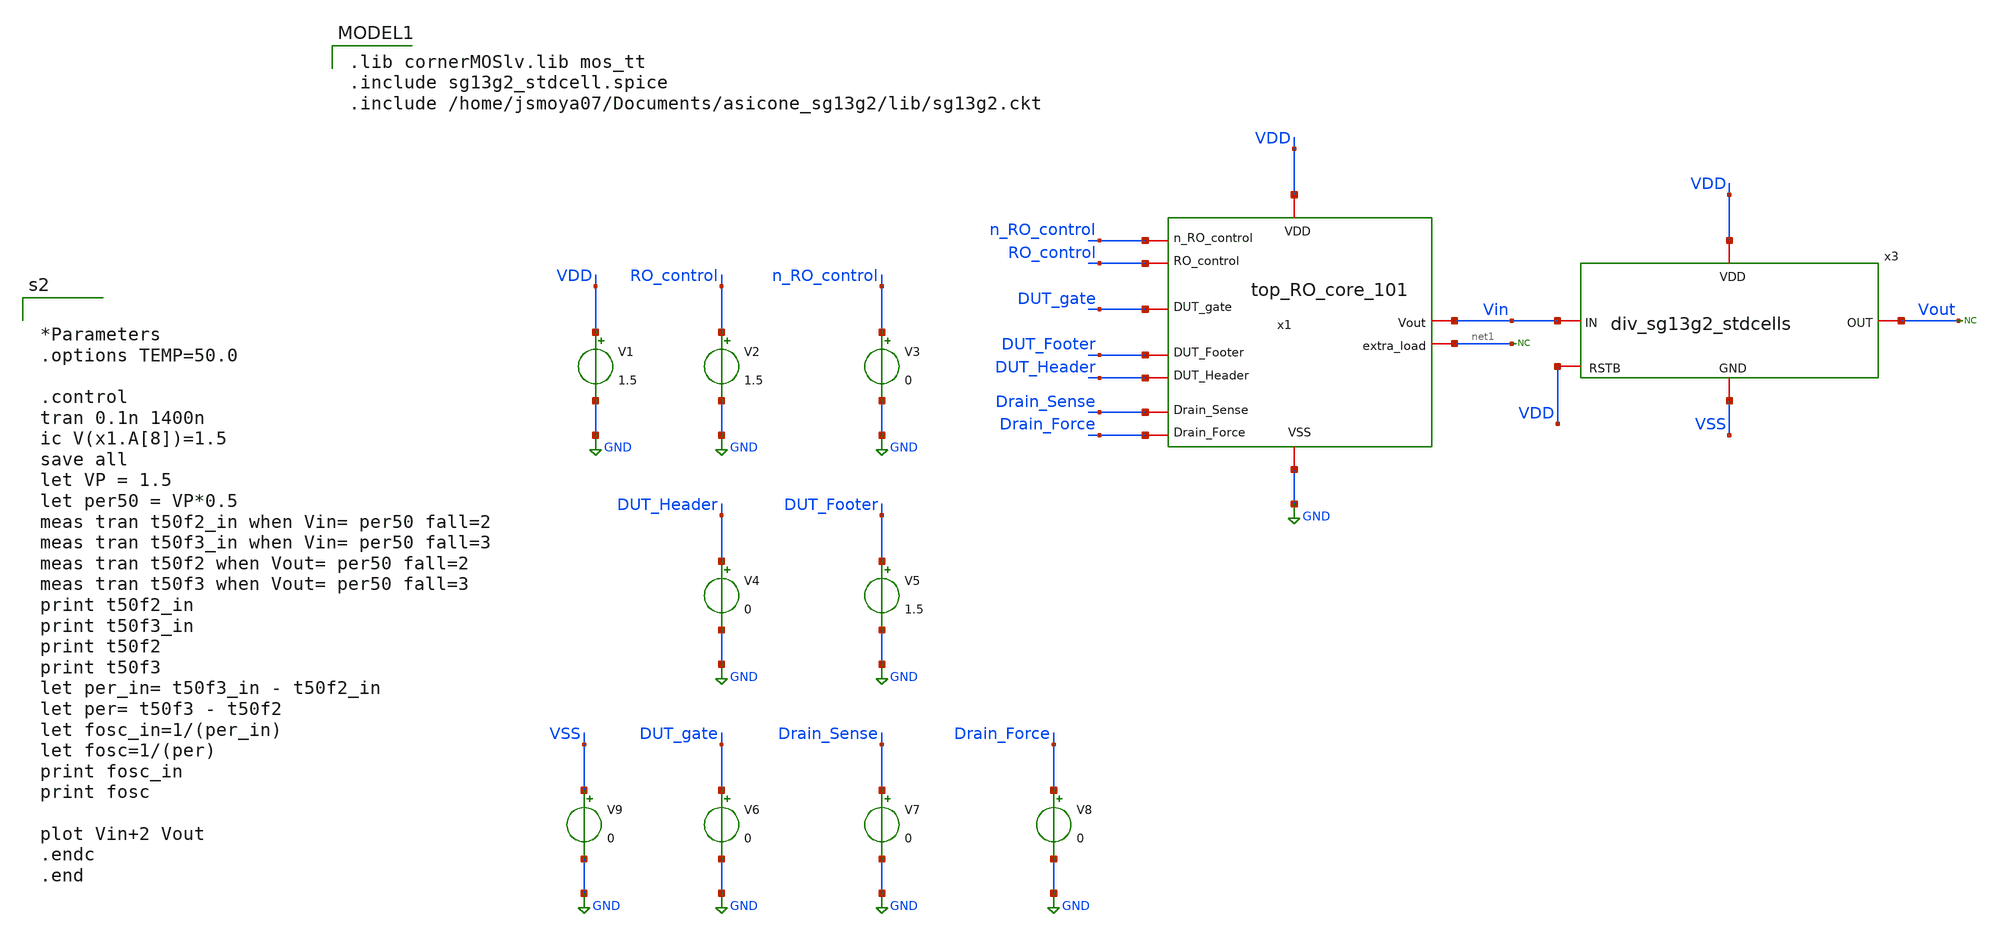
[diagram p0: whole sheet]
** sch_path: unic_cass_wrapper_user_project/ROs_reliability/top_RO_core_101_tb.sch
**.subckt top_RO_core_101_tb
V1 VDD GND 1.5
V2 RO_control GND 1.5
V3 n_RO_control GND 0
V4 DUT_Header GND 0
V5 DUT_Footer GND 1.5
* noconn #net1
V6 DUT_gate GND 0
V7 Drain_Sense GND 0
V8 Drain_Force GND 0
x1 VDD GND n_RO_control RO_control DUT_gate Vin DUT_Header DUT_Footer Drain_Force Drain_Sense net1
+ top_RO_core_101
* noconn Vout
x3 VDD Vout Vin VSS VDD div_sg13g2_stdcells
V9 VSS GND 0
**** begin user architecture code


.ic V(x1.A[8])=0.8
.tran 0.1n 50n
.save all



 .lib cornerMOSlv.lib mos_tt
.include sg13g2_stdcell.spice
.include /home/jsmoya07/Documents/asicone_sg13g2/lib/sg13g2.ckt



*Parameters
.options TEMP=50.0

.control
tran 0.1n 1400n
ic V(x1.A[8])=1.5
save all
let VP = 1.5
let per50 = VP*0.5
meas tran t50f2_in when Vin= per50 fall=2
meas tran t50f3_in when Vin= per50 fall=3
meas tran t50f2 when Vout= per50 fall=2
meas tran t50f3 when Vout= per50 fall=3
print t50f2_in
print t50f3_in
print t50f2
print t50f3
let per_in= t50f3_in - t50f2_in
let per= t50f3 - t50f2
let fosc_in=1/(per_in)
let fosc=1/(per)
print fosc_in
print fosc

plot Vin+2 Vout
.endc
.end


**** end user architecture code
**.ends

* expanding   symbol:  top_RO_core_101.sym # of pins=11
** sym_path: top_RO_core_101.sym
** sch_path: top_RO_core_101.sch
.subckt top_RO_core_101 VDD VSS n_RO_control RO_control DUT_gate Vout DUT_Header DUT_Footer
+ Drain_Force Drain_Sense extra_load
*.iopin VDD
*.iopin VSS
*.iopin n_RO_control
*.iopin RO_control
*.iopin DUT_gate
*.iopin extra_load
*.iopin DUT_Header
*.iopin DUT_Footer
*.iopin Drain_Force
*.iopin Drain_Sense
*.iopin Vout
x1 VDD VSS A[97] A[96] rovcel2
x7 VDD VSS Vout A[100] rovcel2
x3[1] VDD VSS A[96] A[95] rovcel2
x3[2] VDD VSS A[95] A[94] rovcel2
x3[3] VDD VSS A[94] A[93] rovcel2
x3[4] VDD VSS A[93] A[92] rovcel2
x3[5] VDD VSS A[92] A[91] rovcel2
x3[6] VDD VSS A[91] A[90] rovcel2
x3[7] VDD VSS A[90] A[89] rovcel2
x3[8] VDD VSS A[89] A[88] rovcel2
x3[9] VDD VSS A[88] A[87] rovcel2
x3[10] VDD VSS A[87] A[86] rovcel2
x3[11] VDD VSS A[86] A[85] rovcel2
x3[12] VDD VSS A[85] A[84] rovcel2
x3[13] VDD VSS A[84] A[83] rovcel2
x3[14] VDD VSS A[83] A[82] rovcel2
x3[15] VDD VSS A[82] A[81] rovcel2
x3[16] VDD VSS A[81] A[80] rovcel2
x3[17] VDD VSS A[80] A[79] rovcel2
x3[18] VDD VSS A[79] A[78] rovcel2
x3[19] VDD VSS A[78] A[77] rovcel2
x3[20] VDD VSS A[77] A[76] rovcel2
x3[21] VDD VSS A[76] A[75] rovcel2
x3[22] VDD VSS A[75] A[74] rovcel2
x3[23] VDD VSS A[74] A[73] rovcel2
x3[24] VDD VSS A[73] A[72] rovcel2
x3[25] VDD VSS A[72] A[71] rovcel2
x3[26] VDD VSS A[71] A[70] rovcel2
x3[27] VDD VSS A[70] A[69] rovcel2
x3[28] VDD VSS A[69] A[68] rovcel2
x3[29] VDD VSS A[68] A[67] rovcel2
x3[30] VDD VSS A[67] A[66] rovcel2
x3[31] VDD VSS A[66] A[65] rovcel2
x3[32] VDD VSS A[65] A[64] rovcel2
x3[33] VDD VSS A[64] A[63] rovcel2
x3[34] VDD VSS A[63] A[62] rovcel2
x3[35] VDD VSS A[62] A[61] rovcel2
x3[36] VDD VSS A[61] A[60] rovcel2
x3[37] VDD VSS A[60] A[59] rovcel2
x3[38] VDD VSS A[59] A[58] rovcel2
x3[39] VDD VSS A[58] A[57] rovcel2
x3[40] VDD VSS A[57] A[56] rovcel2
x3[41] VDD VSS A[56] A[55] rovcel2
x3[42] VDD VSS A[55] A[54] rovcel2
x3[43] VDD VSS A[54] A[53] rovcel2
x3[44] VDD VSS A[53] A[52] rovcel2
x3[45] VDD VSS A[52] A[51] rovcel2
x3[46] VDD VSS A[51] A[50] rovcel2
x3[47] VDD VSS A[50] A[49] rovcel2
x3[48] VDD VSS A[49] A[48] rovcel2
x3[49] VDD VSS A[48] A[47] rovcel2
x3[50] VDD VSS A[47] A[46] rovcel2
x3[51] VDD VSS A[46] A[45] rovcel2
x3[52] VDD VSS A[45] A[44] rovcel2
x3[53] VDD VSS A[44] A[43] rovcel2
x3[54] VDD VSS A[43] A[42] rovcel2
x3[55] VDD VSS A[42] A[41] rovcel2
x3[56] VDD VSS A[41] A[40] rovcel2
x3[57] VDD VSS A[40] A[39] rovcel2
x3[58] VDD VSS A[39] A[38] rovcel2
x3[59] VDD VSS A[38] A[37] rovcel2
x3[60] VDD VSS A[37] A[36] rovcel2
x3[61] VDD VSS A[36] A[35] rovcel2
x3[62] VDD VSS A[35] A[34] rovcel2
x3[63] VDD VSS A[34] A[33] rovcel2
x3[64] VDD VSS A[33] A[32] rovcel2
x3[65] VDD VSS A[32] A[31] rovcel2
x3[66] VDD VSS A[31] A[30] rovcel2
x3[67] VDD VSS A[30] A[29] rovcel2
x3[68] VDD VSS A[29] A[28] rovcel2
x3[69] VDD VSS A[28] A[27] rovcel2
x3[70] VDD VSS A[27] A[26] rovcel2
x3[71] VDD VSS A[26] A[25] rovcel2
x3[72] VDD VSS A[25] A[24] rovcel2
x3[73] VDD VSS A[24] A[23] rovcel2
x3[74] VDD VSS A[23] A[22] rovcel2
x3[75] VDD VSS A[22] A[21] rovcel2
x3[76] VDD VSS A[21] A[20] rovcel2
x3[77] VDD VSS A[20] A[19] rovcel2
x3[78] VDD VSS A[19] A[18] rovcel2
x3[79] VDD VSS A[18] A[17] rovcel2
x3[80] VDD VSS A[17] A[16] rovcel2
x3[81] VDD VSS A[16] A[15] rovcel2
x3[82] VDD VSS A[15] A[14] rovcel2
x3[83] VDD VSS A[14] A[13] rovcel2
x3[84] VDD VSS A[13] A[12] rovcel2
x3[85] VDD VSS A[12] A[11] rovcel2
x3[86] VDD VSS A[11] A[10] rovcel2
x3[87] VDD VSS A[10] A[9] rovcel2
x3[88] VDD VSS A[9] A[8] rovcel2
x3[89] VDD VSS A[8] A[7] rovcel2
x3[90] VDD VSS A[7] A[6] rovcel2
x3[91] VDD VSS A[6] A[5] rovcel2
x3[92] VDD VSS A[5] A[4] rovcel2
x3[93] VDD VSS A[4] A[3] rovcel2
x3[94] VDD VSS A[3] A[2] rovcel2
x3[95] VDD VSS A[2] A[1] rovcel2
x3[96] VDD VSS A[1] Vout rovcel2
x3 VDD VSS A[97] n_RO_control A[98] RO_control DUT_gate rovcel3
x2 DUT_Header DUT_Footer Drain_Force Drain_Sense RO_control n_RO_control VDD VSS A[98] extra_load
+ rovcel1
x4 VDD VSS extra_load n_RO_control A[100] rovcel4
.ends


* expanding   symbol:  /home/jsmoya07/Documents/RO_reliability/xschem/div_sg13g2_stdcells.sym # of
*+ pins=5
** sym_path: unic_cass_wrapper_user_project/ROs_reliability/div_sg13g2_stdcells.sym
** sch_path: unic_cass_wrapper_user_project/ROs_reliability/div_sg13g2_stdcells.sch
.subckt div_sg13g2_stdcells VDD OUT IN GND RSTB
*.iopin GND
*.iopin IN
*.iopin VDD
*.iopin OUT
*.iopin RSTB
x2 q2 qn2 q1 qn2 RSTB VDD GND sg13g2_dfrbp_1
x1 q1 qn1 IN qn1 RSTB VDD GND sg13g2_dfrbp_1
x3 q3 qn3 q2 qn3 RSTB VDD GND sg13g2_dfrbp_1
x4 q4 qn4 q3 qn4 RSTB VDD GND sg13g2_dfrbp_1
x5 OUT qn5 q4 qn5 RSTB VDD GND sg13g2_dfrbp_1
.ends


* expanding   symbol:  rovcel2.sym # of pins=4
** sym_path: rovcel2.sym
** sch_path: rovcel2.sch
.subckt rovcel2 VDD VSS Vout Vin
*.iopin VDD
*.iopin VSS
*.iopin Vin
*.iopin Vout
* noconn #net1
* noconn #net2
x5 VDD Vin Vout VSS inverter_RO_rel
x1 VDD VDD Vout net2 VSS VSS tgate
x3 VDD VDD Vout net1 VSS VSS tgate
.ends


* expanding   symbol:  rovcel3.sym # of pins=7
** sym_path: rovcel3.sym
** sch_path: rovcel3.sch
.subckt rovcel3 VDD VSS Vin n_RO_control Vout RO_control DUT_gate
*.iopin VDD
*.iopin VSS
*.iopin Vin
*.iopin n_RO_control
*.iopin RO_control
*.iopin DUT_gate
*.iopin Vout
* noconn #net1
x4 VDD VSS Vin n_RO_control RO_control Vout tristate_inv
x1 RO_control VDD Vout net1 VSS n_RO_control tgate
x5 RO_control VDD Vout DUT_gate VSS n_RO_control tgate
.ends


* expanding   symbol:  rovcel1.sym # of pins=10
** sym_path: rovcel1.sym
** sch_path: rovcel1.sch
.subckt rovcel1 DUT_Header DUT_Footer Drain_Force Drain_Sense RO_control n_RO_control VDD VSS Vin
+ Vout
*.iopin VDD
*.iopin VSS
*.iopin Vin
*.iopin DUT_Header
*.iopin DUT_Footer
*.iopin Drain_Force
*.iopin Vout
*.iopin Drain_Sense
*.iopin RO_control
*.iopin n_RO_control
x4 VDD VSS Vin DUT_Header DUT_Footer Vout tristate_inv
x1 RO_control VDD Vout Drain_Force VSS n_RO_control tgate_force
x3 RO_control VDD Vout Drain_Sense VSS n_RO_control tgate
.ends


* expanding   symbol:  rovcel4.sym # of pins=5
** sym_path: rovcel4.sym
** sch_path: rovcel4.sch
.subckt rovcel4 VDD VSS Vin n_RO_control Vout
*.iopin VDD
*.iopin VSS
*.iopin Vin
*.iopin n_RO_control
*.iopin Vout
* noconn #net1
x4 n_RO_control VDD VSS Vin Vout inv1
x1 VDD VDD Vout VSS VSS VSS tgate
x5 VDD VDD Vout net1 VSS VSS tgate
.ends


* expanding   symbol:  sg13g2_stdcells/sg13g2_dfrbp_1.sym # of pins=5
** sym_path: sg13g2_stdcells/sg13g2_dfrbp_1.sym
** sch_path: sg13g2_stdcells/sg13g2_dfrbp_1.sch
.subckt sg13g2_dfrbp_1 Q Q_N CLK D RESET_B VDD VSS
*.ipin D
*.ipin RESET_B
*.ipin CLK
*.opin Q
*.opin Q_N
*.iopin VDD
*.iopin VSS
XM1 Db D net10 VSS sg13_lv_nmos w=420.00n l=130.00n ng=1 m=1 mm_ok=1
XM2 net10 RESET_B VSS VSS sg13_lv_nmos w=420.00n l=130.00n ng=1 m=1 mm_ok=1
XM3 net1 clkneg net9 VSS sg13_lv_nmos w=420.00n l=130.00n ng=1 m=1 mm_ok=1
XM4 net9 net1 VSS VSS sg13_lv_nmos w=420.00n l=130.00n ng=1 m=1 mm_ok=1
XM5 net1 net1 net5 VSS sg13_lv_nmos w=420.00n l=130.00n ng=1 m=1 mm_ok=1
XM6 net5 RESET_B VSS VSS sg13_lv_nmos w=420.00n l=130.00n ng=1 m=1 mm_ok=1
XM7 Q_N net1 VSS VSS sg13_lv_nmos w=740.00n l=130.00n ng=1 m=1 mm_ok=1
XM8 net2 net1 VSS VSS sg13_lv_nmos w=740.00n l=130.00n ng=1 m=1 mm_ok=1
XM9 Q net2 VSS VSS sg13_lv_nmos w=740.00n l=130.00n ng=1 m=1 mm_ok=1
XM10 clkneg CLK VSS VSS sg13_lv_nmos w=740.00n l=130.00n ng=1 m=1 mm_ok=1
XM11 clkpos clkneg VSS VSS sg13_lv_nmos w=740.00n l=130.00n ng=1 m=1 mm_ok=1
XM12 Db clkneg net3 VSS sg13_lv_nmos w=420.00n l=130.00n ng=1 m=1 mm_ok=1
XM13 net3 clkpos net8 VSS sg13_lv_nmos w=420.00n l=130.00n ng=1 m=1 mm_ok=1
XM14 net8 net3 net4 VSS sg13_lv_nmos w=420.00n l=130.00n ng=1 m=1 mm_ok=1
XM15 net4 RESET_B VSS VSS sg13_lv_nmos w=420.00n l=130.00n ng=1 m=1 mm_ok=1
XM16 net3 net3 VSS VSS sg13_lv_nmos w=740.00n l=130.00n ng=1 m=1 mm_ok=1
XM17 net3 clkpos net1 VSS sg13_lv_nmos w=740.00n l=130.00n ng=1 m=1 mm_ok=1
XM18 Db RESET_B VDD VDD sg13_lv_pmos w=420.00n l=130.00n ng=1 m=1 mm_ok=1
XM19 Db D VDD VDD sg13_lv_pmos w=420.00n l=130.00n ng=1 m=1 mm_ok=1
XM20 net7 net1 VDD VDD sg13_lv_pmos w=420.00n l=130.00n ng=1 m=1 mm_ok=1
XM21 net1 clkpos net7 VDD sg13_lv_pmos w=420.00n l=130.00n ng=1 m=1 mm_ok=1
XM22 net1 net1 VDD VDD sg13_lv_pmos w=420.00n l=130.00n ng=1 m=1 mm_ok=1
XM23 net1 RESET_B VDD VDD sg13_lv_pmos w=420.00n l=130.00n ng=1 m=1 mm_ok=1
XM24 Q_N net1 VDD VDD sg13_lv_pmos w=1.12u l=130.00n ng=1 m=1 mm_ok=1
XM25 net2 net1 VDD VDD sg13_lv_pmos w=1.12u l=130.00n ng=1 m=1 mm_ok=1
XM26 Q net2 VDD VDD sg13_lv_pmos w=1.12u l=130.00n ng=1 m=1 mm_ok=1
XM27 clkneg CLK VDD VDD sg13_lv_pmos w=1.12u l=130.00n ng=1 m=1 mm_ok=1
XM28 clkpos clkneg VDD VDD sg13_lv_pmos w=1.12u l=130.00n ng=1 m=1 mm_ok=1
XM29 Db clkpos net3 VDD sg13_lv_pmos w=420.00n l=130.00n ng=1 m=1 mm_ok=1
XM30 net6 net3 VDD VDD sg13_lv_pmos w=420.00n l=130.00n ng=1 m=1 mm_ok=1
XM31 net3 clkneg net6 VDD sg13_lv_pmos w=420.00n l=130.00n ng=1 m=1 mm_ok=1
XM32 net3 RESET_B VDD VDD sg13_lv_pmos w=420.00n l=130.00n ng=1 m=1 mm_ok=1
XM33 net3 net3 VDD VDD sg13_lv_pmos w=1.000u l=130.00n ng=1 m=1 mm_ok=1
XM34 net3 clkneg net1 VDD sg13_lv_pmos w=1.000u l=130.00n ng=1 m=1 mm_ok=1
.ends


* expanding   symbol:  inverter_RO_rel.sym # of pins=4
** sym_path: inverter_RO_rel.sym
** sch_path: inverter_RO_rel.sch
.subckt inverter_RO_rel VDD Vin Vout VSS
*.iopin VDD
*.iopin VSS
*.iopin Vin
*.iopin Vout
XM3 Vout Vin VDD VDD sg13_lv_pmos w=3.4u l=0.45u ng=1 m=4 mm_ok=1
XM1 VSS Vin Vout VSS sg13_lv_nmos w=1.3u l=0.45u ng=1 m=4 mm_ok=1
.ends


* expanding   symbol:  tgate.sym # of pins=6
** sym_path: tgate.sym
** sch_path: tgate.sch
.subckt tgate nclk VDD Vin Vout VSS clk
*.iopin nclk
*.iopin clk
*.iopin VDD
*.iopin VSS
*.iopin Vout
*.iopin Vin
XM3 Vout nclk Vin VDD sg13_lv_pmos w=3.4u l=0.45u ng=1 m=1 mm_ok=1
XM1 Vout clk Vin VSS sg13_lv_nmos w=1.3u l=0.45u ng=1 m=1 mm_ok=1
.ends


* expanding   symbol:  tristate_inv.sym # of pins=6
** sym_path: tristate_inv.sym
** sch_path: tristate_inv.sch
.subckt tristate_inv VDD VSS Vin Vup Vdn Vout
*.iopin VDD
*.iopin VSS
*.iopin Vin
*.iopin Vout
*.iopin Vup
*.iopin Vdn
XM5 Vout Vin net1 VDD sg13_lv_pmos w=3.4u l=0.45u ng=1 m=4 mm_ok=1
XM2 net2 Vin Vout VSS sg13_lv_nmos w=1.3u l=0.45u ng=1 m=4 mm_ok=1
XM1 net1 Vup VDD VDD sg13_lv_pmos w=3.4u l=0.45u ng=1 m=12 mm_ok=1
XM3 VSS Vdn net2 VSS sg13_lv_nmos w=1.3u l=0.45u ng=1 m=12 mm_ok=1
.ends


* expanding   symbol:  tgate_force.sym # of pins=6
** sym_path: tgate_force.sym
** sch_path: tgate_force.sch
.subckt tgate_force nclk VDD Vin Vout VSS clk
*.iopin nclk
*.iopin clk
*.iopin VDD
*.iopin VSS
*.iopin Vout
*.iopin Vin
XM3 Vout nclk Vin VDD sg13_lv_pmos w=3.4u l=0.45u ng=1 m=4 mm_ok=1
XM4 Vout clk Vin VSS sg13_lv_nmos w=1.3u l=0.45u ng=1 m=4 mm_ok=1
.ends


* expanding   symbol:  inv1.sym # of pins=5
** sym_path: inv1.sym
** sch_path: inv1.sch
.subckt inv1 n_RO_control VDD VSS Vin Vout
*.iopin VDD
*.iopin VSS
*.iopin Vin
*.iopin Vout
*.iopin n_RO_control
XM1 net1 n_RO_control VDD VDD sg13_lv_pmos w=3.4u l=0.45u ng=1 m=12 mm_ok=1
XM5 Vout Vin net1 VDD sg13_lv_pmos w=3.4u l=0.45u ng=1 m=4 mm_ok=1
XM2 VSS Vin Vout VSS sg13_lv_nmos w=1.3u l=0.45u ng=1 m=4 mm_ok=1
.ends

.GLOBAL GND
.end
